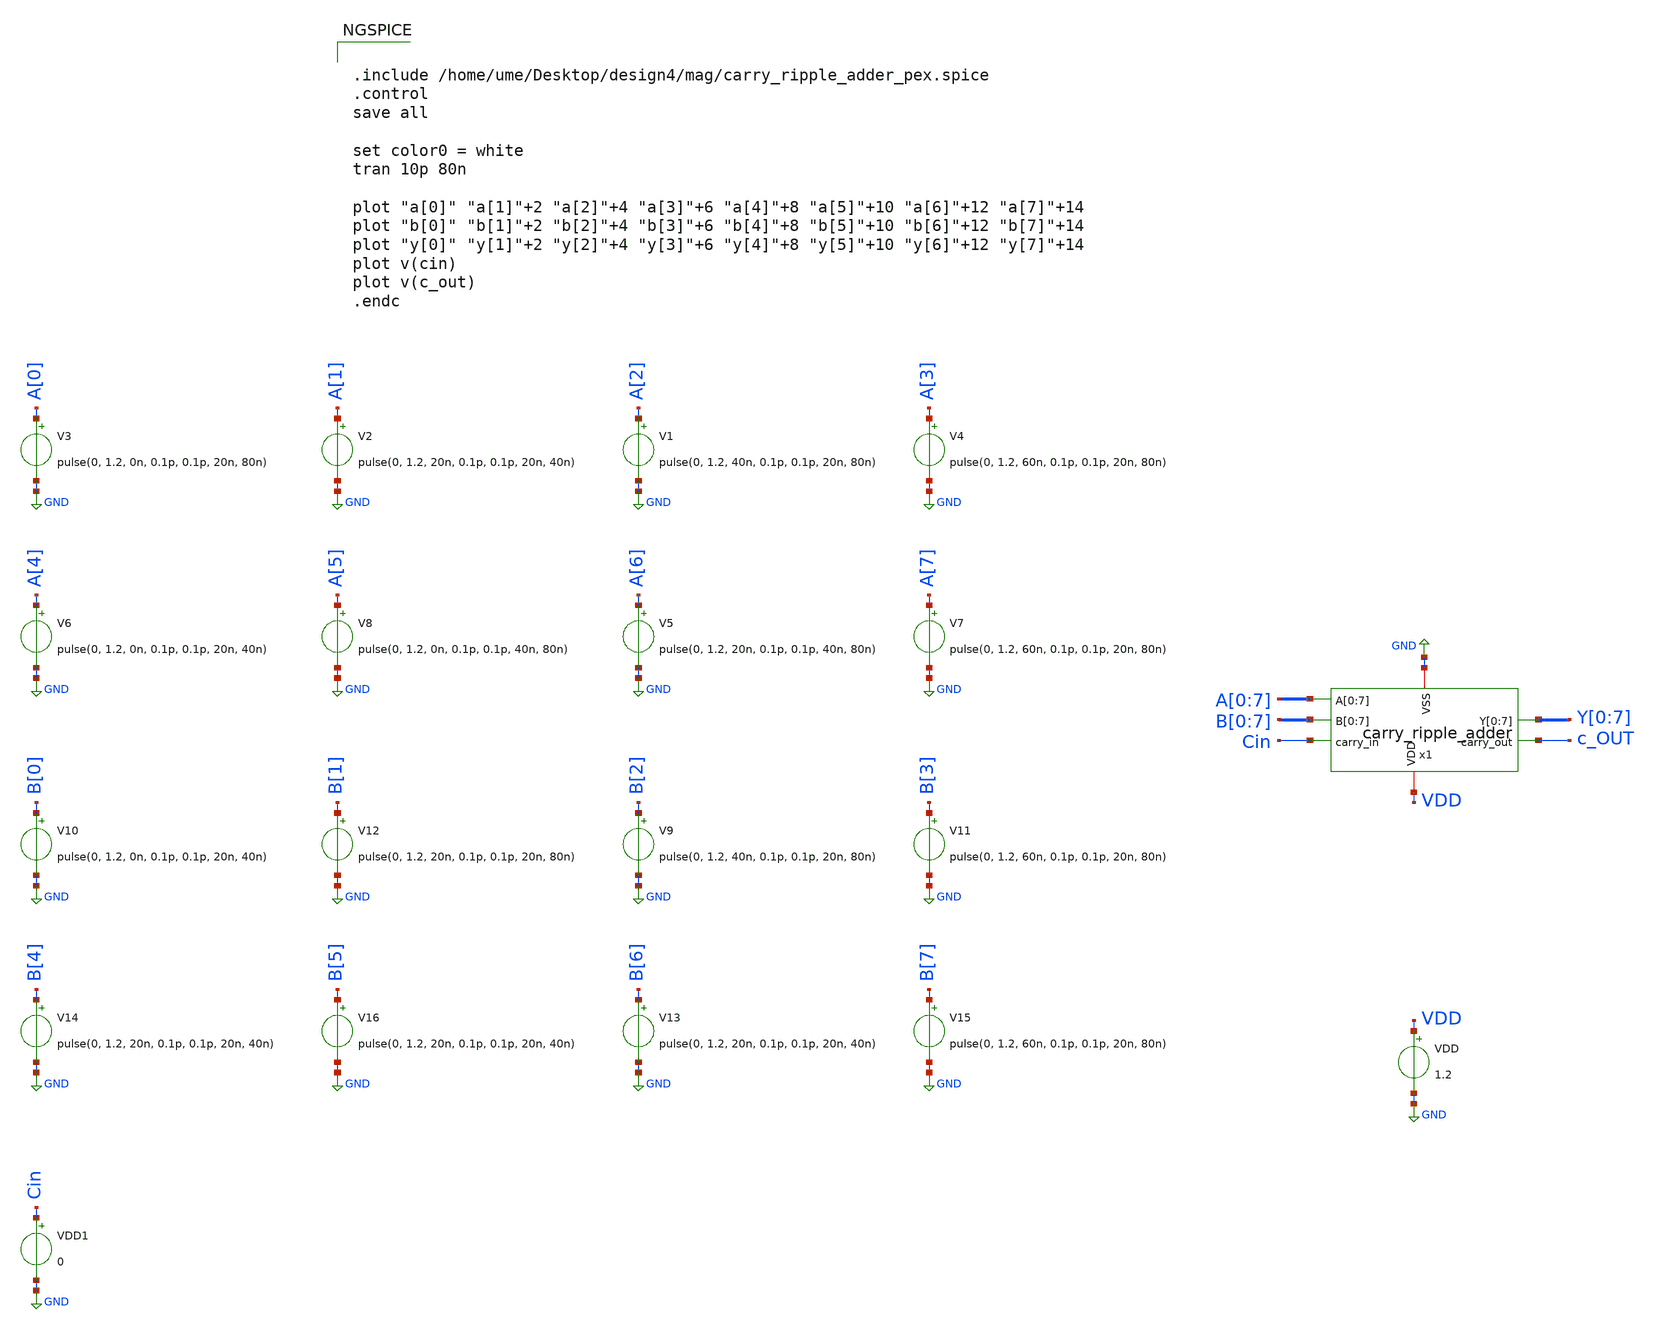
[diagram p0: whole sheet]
** sch_path: design/RIPPLE_CARRY_ADDER/xschem/carry_ripple_adder_tb.sch
**.subckt carry_ripple_adder_tb
x1 A[0] A[1] A[2] A[3] A[4] A[5] A[6] A[7] B[0] B[1] B[2] B[3] B[4] B[5] B[6] B[7] Cin VDD GND Y[0]
+ Y[1] Y[2] Y[3] Y[4] Y[5] Y[6] Y[7] c_OUT carry_ripple_adder
V1 A[2] GND pulse(0, 1.2, 40n, 0.1p, 0.1p, 20n, 80n)
V3 A[0] GND pulse(0, 1.2, 0n, 0.1p, 0.1p, 20n, 80n)
V4 A[3] GND pulse(0, 1.2, 60n, 0.1p, 0.1p, 20n, 80n)
V2 A[1] GND pulse(0, 1.2, 20n, 0.1p, 0.1p, 20n, 40n)
V5 A[6] GND pulse(0, 1.2, 20n, 0.1p, 0.1p, 40n, 80n)
V6 A[4] GND pulse(0, 1.2, 0n, 0.1p, 0.1p, 20n, 40n)
V7 A[7] GND pulse(0, 1.2, 60n, 0.1p, 0.1p, 20n, 80n)
V8 A[5] GND pulse(0, 1.2, 0n, 0.1p, 0.1p, 40n, 80n)
V9 B[2] GND pulse(0, 1.2, 40n, 0.1p, 0.1p, 20n, 80n)
V11 B[3] GND pulse(0, 1.2, 60n, 0.1p, 0.1p, 20n, 80n)
V12 B[1] GND pulse(0, 1.2, 20n, 0.1p, 0.1p, 20n, 80n)
V15 B[7] GND pulse(0, 1.2, 60n, 0.1p, 0.1p, 20n, 80n)
V10 B[0] GND pulse(0, 1.2, 0n, 0.1p, 0.1p, 20n, 40n)
V16 B[5] GND pulse(0, 1.2, 20n, 0.1p, 0.1p, 20n, 40n)
VDD VDD GND 1.2
V14 B[4] GND pulse(0, 1.2, 20n, 0.1p, 0.1p, 20n, 40n)
V13 B[6] GND pulse(0, 1.2, 20n, 0.1p, 0.1p, 20n, 40n)
VDD1 Cin GND 0
**** begin user architecture code


.include /home/ume/Desktop/design4/mag/carry_ripple_adder_pex.spice
.control
save all

set color0 = white
tran 10p 80n

plot "a[0]" "a[1]"+2 "a[2]"+4 "a[3]"+6 "a[4]"+8 "a[5]"+10 "a[6]"+12 "a[7]"+14
plot "b[0]" "b[1]"+2 "b[2]"+4 "b[3]"+6 "b[4]"+8 "b[5]"+10 "b[6]"+12 "b[7]"+14
plot "y[0]" "y[1]"+2 "y[2]"+4 "y[3]"+6 "y[4]"+8 "y[5]"+10 "y[6]"+12 "y[7]"+14
plot v(cin)
plot v(c_out)
.endc


** opencircuitdesign pdks install
.lib $::SKYWATER_MODELS/sky130.lib.spice tt_mm


**** end user architecture code
**.ends
.GLOBAL GND
.end
